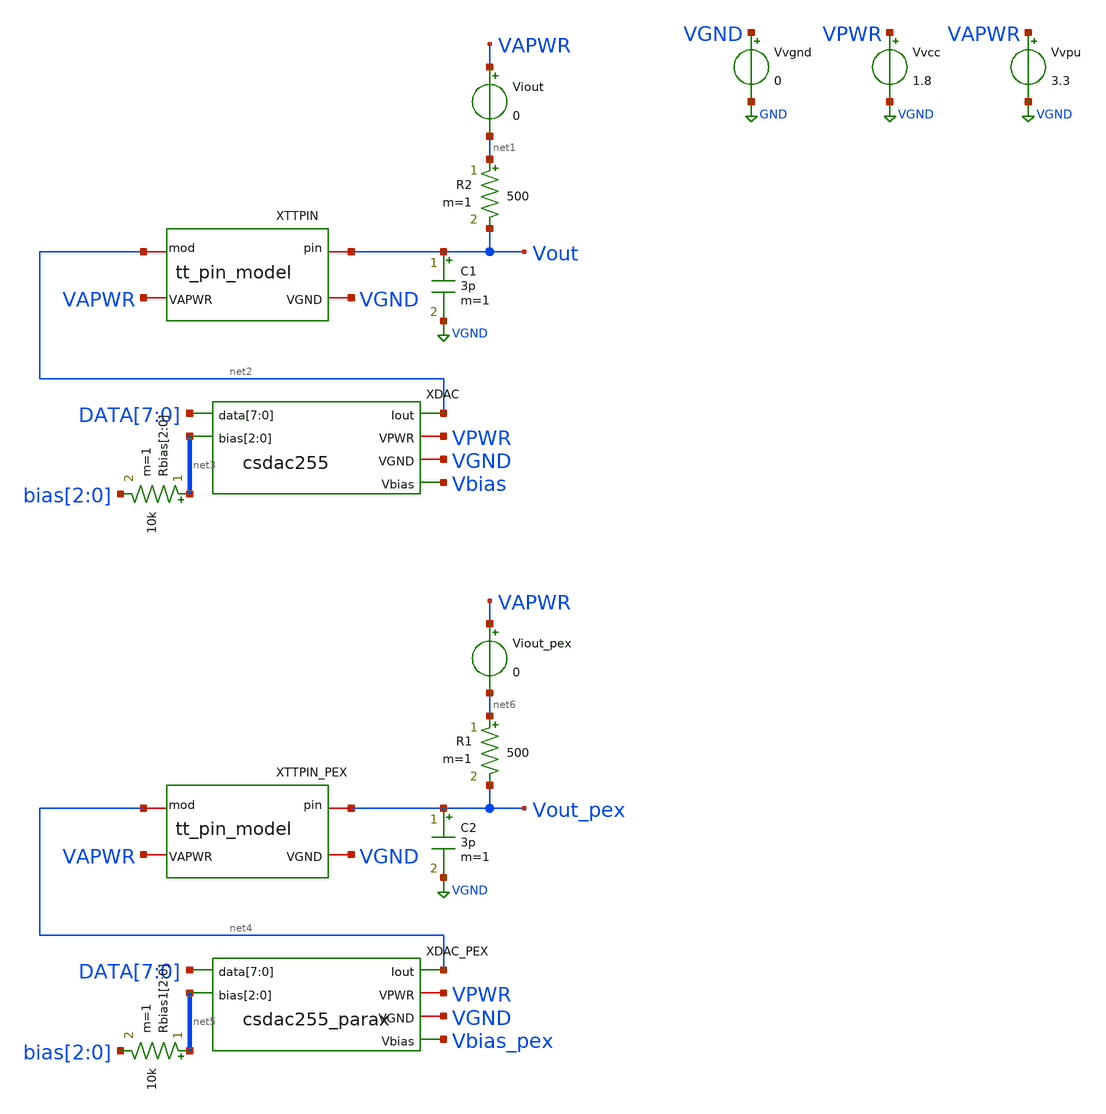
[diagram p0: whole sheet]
** sch_path: xschem/tb_csdac255.sch
**.subckt tb_csdac255
Vvcc VPWR VGND 1.8
Vvpu VAPWR VGND 3.3
Vvgnd VGND GND 0
XDAC DATA[7] DATA[6] DATA[5] DATA[4] DATA[3] DATA[2] DATA[1] DATA[0] net2 VPWR VGND Vbias net3[2]
+ net3[1] net3[0] csdac255
XTTPIN VGND VAPWR net2 Vout tt_pin_model
R2 net1 Vout 500 m=1
Viout VAPWR net1 0
C1 Vout VGND 3p m=1
Rbias[2] net3[2] bias[2] 10k m=1
Rbias[1] net3[1] bias[1] 10k m=1
Rbias[0] net3[0] bias[0] 10k m=1
XDAC_PEX DATA[7] DATA[6] DATA[5] DATA[4] DATA[3] DATA[2] DATA[1] DATA[0] net4 VPWR VGND Vbias_pex
+ net5[2] net5[1] net5[0] csdac255_parax
Rbias1[2] net5[2] bias[2] 10k m=1
Rbias1[1] net5[1] bias[1] 10k m=1
Rbias1[0] net5[0] bias[0] 10k m=1
XTTPIN_PEX VGND VAPWR net4 Vout_pex tt_pin_model
R1 net6 Vout_pex 500 m=1
Viout_pex VAPWR net6 0
C2 Vout_pex VGND 3p m=1
**** begin user architecture code



* Set Vbias level (negative logic, so 0=ON, 1.8=OFF):
.param bias2=1.8
.param bias1=1.8
.param bias0=1.8
Vvbias2 bias[2] GND {bias2}
Vvbias1 bias[1] GND {bias1}
Vvbias0 bias[0] GND {bias0}

*NOTE: Possible ngspice bug with .IF(), so it's commented out here:
*.param singlebits=0
*.IF (singlebits == 1)
* Mode to just test each binary-weighted level:
*Vxp0 DATA[0]  GND pulse 0v 1.8v 1u 1n 1n 1u 10u
*Vxp1 DATA[1]  GND pulse 0v 1.8v 2u 1n 1n 1u 10u
*Vxp2 DATA[2]  GND pulse 0v 1.8v 3u 1n 1n 1u 10u
*Vxp3 DATA[3]  GND pulse 0v 1.8v 4u 1n 1n 1u 10u
*Vxp4 DATA[4]  GND pulse 0v 1.8v 5u 1n 1n 1u 10u
*Vxp5 DATA[5]  GND pulse 0v 1.8v 6u 1n 1n 1u 10u
*Vxp6 DATA[6]  GND pulse 0v 1.8v 7u 1n 1n 1u 10u
*Vxp7 DATA[7]  GND pulse 0v 1.8v 8u 1n 1n 1u 10u
*.ELSEIF (singlebits == 0)
* Mode to test full 0..255 trange:
Vxp0 DATA[0]  GND pulse 1.8v 0v 0n 1n 1n 39n 80n
Vxp1 DATA[1]  GND pulse 1.8v 0v 0n 1n 1n 79n 160n
Vxp2 DATA[2]  GND pulse 1.8v 0v 0n 1n 1n 159n 320n
Vxp3 DATA[3]  GND pulse 1.8v 0v 0n 1n 1n 319n 640n
Vxp4 DATA[4]  GND pulse 1.8v 0v 0n 1n 1n 639n 1280n
Vxp5 DATA[5]  GND pulse 1.8v 0v 0n 1n 1n 1279n 2560n
Vxp6 DATA[6]  GND pulse 1.8v 0v 0n 1n 1n 2559n 5120n
Vxp7 DATA[7]  GND pulse 1.8v 0v 0n 1n 1n 5119n 10240n
*.endif

*.options savecurrents
.control
	* Start with all bias[*] switches at 0V (ENb), so highest Vbias (max current sink):
	let biaslevel=7
	foreach bv2 0 1.8
		foreach bv1 0 1.8
			foreach bv0 0 1.8
				alterparam bias2 = $bv2
				alterparam bias1 = $bv1
				alterparam bias0 = $bv0
				reset
				echo Bias level $&biaslevel = $bv2 $bv1 $bv0
				save
				+ data[0] data[1] data[2] data[3] data[4] data[5] data[6] data[7]
				+ bias[0] bias[1] bias[2]
				+ vbias          vbias_pex
				+ vout i(viout)  vout_pex i(viout_pex)
				+ i(vvcc)
				+ i(vvpu)
				+ i(vvgnd)
				+ XDAC.THERMO_ROWn[0] XDAC.THERMO_ROWn[1] XDAC.THERMO_ROWn[2] XDAC.THERMO_ROWn[3] XDAC.THERMO_ROWn[4] XDAC.THERMO_ROWn[5] XDAC.THERMO_ROWn[6] XDAC.THERMO_ROWn[7] XDAC.THERMO_ROWn[8] XDAC.THERMO_ROWn[9] XDAC.THERMO_ROWn[10] XDAC.THERMO_ROWn[11] XDAC.THERMO_ROWn[12] XDAC.THERMO_ROWn[13] XDAC.THERMO_ROWn[14]
				+ XDAC.THERMO_COLn[0] XDAC.THERMO_COLn[1] XDAC.THERMO_COLn[2] XDAC.THERMO_COLn[3] XDAC.THERMO_COLn[4] XDAC.THERMO_COLn[5] XDAC.THERMO_COLn[6] XDAC.THERMO_COLn[7] XDAC.THERMO_COLn[8] XDAC.THERMO_COLn[9] XDAC.THERMO_COLn[10] XDAC.THERMO_COLn[11] XDAC.THERMO_COLn[12] XDAC.THERMO_COLn[13] XDAC.THERMO_COLn[14]
				+ XDAC.XThR.TA1 XDAC.XThR.TA2 XDAC.XThR.TA3 XDAC.XThR.TAN XDAC.XThR.TAN2 XDAC.XThR.TB1 XDAC.XThR.TB2 XDAC.XThR.TB3 XDAC.XThR.TB4 XDAC.XThR.TB5 XDAC.XThR.TB6 XDAC.XThR.TB7 XDAC.XThR.TBN
				+ XDAC.XThC.TA1 XDAC.XThC.TA2 XDAC.XThC.TA3 XDAC.XThC.TAN XDAC.XThC.TAN2 XDAC.XThC.TB1 XDAC.XThC.TB2 XDAC.XThC.TB3 XDAC.XThC.TB4 XDAC.XThC.TB5 XDAC.XThC.TB6 XDAC.XThC.TB7 XDAC.XThC.TBN
				+ XDAC_PEX.XThR.Tn[0] XDAC_PEX.XThR.Tn[1] XDAC_PEX.XThR.Tn[2] XDAC_PEX.XThR.Tn[3] XDAC_PEX.XThR.Tn[4] XDAC_PEX.XThR.Tn[5] XDAC_PEX.XThR.Tn[6] XDAC_PEX.XThR.Tn[7] XDAC_PEX.XThR.Tn[8] XDAC_PEX.XThR.Tn[9] XDAC_PEX.XThR.Tn[10] XDAC_PEX.XThR.Tn[11] XDAC_PEX.XThR.Tn[12] XDAC_PEX.XThR.Tn[13] XDAC_PEX.XThR.Tn[14]
				+ XDAC_PEX.XThC.Tn[0] XDAC_PEX.XThC.Tn[1] XDAC_PEX.XThC.Tn[2] XDAC_PEX.XThC.Tn[3] XDAC_PEX.XThC.Tn[4] XDAC_PEX.XThC.Tn[5] XDAC_PEX.XThC.Tn[6] XDAC_PEX.XThC.Tn[7] XDAC_PEX.XThC.Tn[8] XDAC_PEX.XThC.Tn[9] XDAC_PEX.XThC.Tn[10] XDAC_PEX.XThC.Tn[11] XDAC_PEX.XThC.Tn[12] XDAC_PEX.XThC.Tn[13] XDAC_PEX.XThC.Tn[14]
				+ XDAC_PEX.XThR.TA1 XDAC_PEX.XThR.TA2 XDAC_PEX.XThR.TA3 XDAC_PEX.XThR.TAN XDAC_PEX.XThR.TAN2 XDAC_PEX.XThR.TB1 XDAC_PEX.XThR.TB2 XDAC_PEX.XThR.TB3 XDAC_PEX.XThR.TB4 XDAC_PEX.XThR.TB5 XDAC_PEX.XThR.TB6 XDAC_PEX.XThR.TB7 XDAC_PEX.XThR.TBN
				+ XDAC_PEX.XThC.TA1 XDAC_PEX.XThC.TA2 XDAC_PEX.XThC.TA3 XDAC_PEX.XThC.TAN XDAC_PEX.XThC.TAN2 XDAC_PEX.XThC.TB1 XDAC_PEX.XThC.TB2 XDAC_PEX.XThC.TB3 XDAC_PEX.XThC.TB4 XDAC_PEX.XThC.TB5 XDAC_PEX.XThC.TB6 XDAC_PEX.XThC.TB7 XDAC_PEX.XThC.TBN
				tran 1n 12.8u
				write tb_csdac255_all.raw
				write tb_csdac255.raw vbias vout i(viout) i(vvgnd) i(vvcc) i(vvpu) vbias_pex vout_pex i(viout_pex)
				+ XDAC.THERMO_ROWn[0] XDAC.THERMO_ROWn[1] XDAC.THERMO_ROWn[2] XDAC.THERMO_ROWn[3] XDAC.THERMO_ROWn[4] XDAC.THERMO_ROWn[5] XDAC.THERMO_ROWn[6] XDAC.THERMO_ROWn[7] XDAC.THERMO_ROWn[8] XDAC.THERMO_ROWn[9] XDAC.THERMO_ROWn[10] XDAC.THERMO_ROWn[11] XDAC.THERMO_ROWn[12] XDAC.THERMO_ROWn[13] XDAC.THERMO_ROWn[14] XDAC.THERMO_COLn[0] XDAC.THERMO_COLn[1] XDAC.THERMO_COLn[2] XDAC.THERMO_COLn[3] XDAC.THERMO_COLn[4] XDAC.THERMO_COLn[5] XDAC.THERMO_COLn[6] XDAC.THERMO_COLn[7] XDAC.THERMO_COLn[8] XDAC.THERMO_COLn[9] XDAC.THERMO_COLn[10] XDAC.THERMO_COLn[11] XDAC.THERMO_COLn[12] XDAC.THERMO_COLn[13] XDAC.THERMO_COLn[14] XDAC.XThR.TA1 XDAC.XThR.TA2 XDAC.XThR.TA3 XDAC.XThR.TAN XDAC.XThR.TAN2 XDAC.XThR.TB1 XDAC.XThR.TB2 XDAC.XThR.TB3 XDAC.XThR.TB4 XDAC.XThR.TB5 XDAC.XThR.TB6 XDAC.XThR.TB7 XDAC.XThR.TBN XDAC.XThC.TA1 XDAC.XThC.TA2 XDAC.XThC.TA3 XDAC.XThC.TAN XDAC.XThC.TAN2 XDAC.XThC.TB1 XDAC.XThC.TB2 XDAC.XThC.TB3 XDAC.XThC.TB4 XDAC.XThC.TB5 XDAC.XThC.TB6 XDAC.XThC.TB7 XDAC.XThC.TBN
				+ XDAC_PEX.XThR.Tn[0] XDAC_PEX.XThR.Tn[1] XDAC_PEX.XThR.Tn[2] XDAC_PEX.XThR.Tn[3] XDAC_PEX.XThR.Tn[4] XDAC_PEX.XThR.Tn[5] XDAC_PEX.XThR.Tn[6] XDAC_PEX.XThR.Tn[7] XDAC_PEX.XThR.Tn[8] XDAC_PEX.XThR.Tn[9] XDAC_PEX.XThR.Tn[10] XDAC_PEX.XThR.Tn[11] XDAC_PEX.XThR.Tn[12] XDAC_PEX.XThR.Tn[13] XDAC_PEX.XThR.Tn[14] XDAC_PEX.XThC.Tn[0] XDAC_PEX.XThC.Tn[1] XDAC_PEX.XThC.Tn[2] XDAC_PEX.XThC.Tn[3] XDAC_PEX.XThC.Tn[4] XDAC_PEX.XThC.Tn[5] XDAC_PEX.XThC.Tn[6] XDAC_PEX.XThC.Tn[7] XDAC_PEX.XThC.Tn[8] XDAC_PEX.XThC.Tn[9] XDAC_PEX.XThC.Tn[10] XDAC_PEX.XThC.Tn[11] XDAC_PEX.XThC.Tn[12] XDAC_PEX.XThC.Tn[13] XDAC_PEX.XThC.Tn[14] XDAC_PEX.XThR.TA1 XDAC_PEX.XThR.TA2 XDAC_PEX.XThR.TA3 XDAC_PEX.XThR.TAN XDAC_PEX.XThR.TAN2 XDAC_PEX.XThR.TB1 XDAC_PEX.XThR.TB2 XDAC_PEX.XThR.TB3 XDAC_PEX.XThR.TB4 XDAC_PEX.XThR.TB5 XDAC_PEX.XThR.TB6 XDAC_PEX.XThR.TB7 XDAC_PEX.XThR.TBN XDAC_PEX.XThC.TA1 XDAC_PEX.XThC.TA2 XDAC_PEX.XThC.TA3 XDAC_PEX.XThC.TAN XDAC_PEX.XThC.TAN2 XDAC_PEX.XThC.TB1 XDAC_PEX.XThC.TB2 XDAC_PEX.XThC.TB3 XDAC_PEX.XThC.TB4 XDAC_PEX.XThC.TB5 XDAC_PEX.XThC.TB6 XDAC_PEX.XThC.TB7 XDAC_PEX.XThC.TBN
				*plot vout vbias i(viout)*1000
				set appendwrite
				reset
				let biaslevel = biaslevel - 1
			end
		end
	end
.endc




.lib /home/anton/asic/ciel/sky130A/libs.tech/combined/sky130.lib.spice tt
.include $::SKYWATER_STDCELLS/sky130_fd_sc_hd.spice

**** end user architecture code
**.ends

* expanding   symbol:  csdac255.sym # of pins=6
** sym_path: xschem/csdac255.sym
** sch_path: xschem/csdac255.sch
.subckt csdac255 data[7] data[6] data[5] data[4] data[3] data[2] data[1] data[0] Iout VPWR VGND Vbias bias[2] bias[1] bias[0]
*.iopin VPWR
*.opin Iout
*.iopin VGND
*.ipin bias[2],bias[1],bias[0]
*.ipin data[7],data[6],data[5],data[4],data[3],data[2],data[1],data[0]
*.opin Vbias
XThR VPWR VGND THERMO_ROWn[14] THERMO_ROWn[13] THERMO_ROWn[12] THERMO_ROWn[11] THERMO_ROWn[10] THERMO_ROWn[9] THERMO_ROWn[8] THERMO_ROWn[7] THERMO_ROWn[6] THERMO_ROWn[5] THERMO_ROWn[4] THERMO_ROWn[3] THERMO_ROWn[2] THERMO_ROWn[1] THERMO_ROWn[0] data[7] data[6] data[5] data[4] thermo15
XA VPWR VGND THERMO_ROWn[14] THERMO_ROWn[13] THERMO_ROWn[12] THERMO_ROWn[11] THERMO_ROWn[10] THERMO_ROWn[9] THERMO_ROWn[8] THERMO_ROWn[7] THERMO_ROWn[6] THERMO_ROWn[5] THERMO_ROWn[4] THERMO_ROWn[3] THERMO_ROWn[2] THERMO_ROWn[1] THERMO_ROWn[0] THERMO_COLn[14] THERMO_COLn[13] THERMO_COLn[12] THERMO_COLn[11] THERMO_COLn[10] THERMO_COLn[9] THERMO_COLn[8] THERMO_COLn[7] THERMO_COLn[6] THERMO_COLn[5] THERMO_COLn[4] THERMO_COLn[3] THERMO_COLn[2] THERMO_COLn[1] THERMO_COLn[0] Vbias Iout array255x
XThC VPWR VGND THERMO_COLn[14] THERMO_COLn[13] THERMO_COLn[12] THERMO_COLn[11] THERMO_COLn[10] THERMO_COLn[9] THERMO_COLn[8] THERMO_COLn[7] THERMO_COLn[6] THERMO_COLn[5] THERMO_COLn[4] THERMO_COLn[3] THERMO_COLn[2] THERMO_COLn[1] THERMO_COLn[0] data[3] data[2] data[1] data[0] thermo15
XVB VPWR VGND bias[2] bias[1] bias[0] Vbias vbias
XCVb Vbias VGND sky130_fd_pr__cap_mim_m3_1 W=11.82 L=4.81 MF=1 m=1
.ends


* expanding   symbol:  tt_pin_model.sym # of pins=4
** sym_path: xschem/tt_pin_model.sym
** sch_path: xschem/tt_pin_model.sch
.subckt tt_pin_model VGND VAPWR mod pin
*.iopin VGND
*.iopin VAPWR
*.iopin mod
*.iopin pin
R2 net1 pin 1 m=1
C2 pin VGND 1p m=1
L7 net2 net1 1n m=1
C3 net2 VGND 2p m=1
R3 net3 net2 50 m=1
C4 net3 VGND 250f m=1
XM2 net3 VGND mod VAPWR sky130_fd_pr__pfet_g5v0d10v5 L=0.5 W=100 nf=20 ad='int((nf+1)/2) * W/nf * 0.29' as='int((nf+2)/2)
+ * W/nf * 0.29' pd='2*int((nf+1)/2) * (W/nf + 0.29)' ps='2*int((nf+2)/2) * (W/nf + 0.29)' nrd='0.29 /
+ W' nrs='0.29 / W' sa=0 sb=0 sd=0 mult=1 m=1
XM1 net3 VAPWR mod VGND sky130_fd_pr__nfet_g5v0d10v5 L=0.5 W=60 nf=12 ad='int((nf+1)/2) * W/nf * 0.29' as='int((nf+2)/2)
+ * W/nf * 0.29' pd='2*int((nf+1)/2) * (W/nf + 0.29)' ps='2*int((nf+2)/2) * (W/nf + 0.29)' nrd='0.29 /
+ W' nrs='0.29 / W' sa=0 sb=0 sd=0 mult=1 m=1
XM4 net3 VAPWR VGND VAPWR sky130_fd_pr__pfet_g5v0d10v5 L=0.5 W=100 nf=20 ad='int((nf+1)/2) * W/nf * 0.29' as='int((nf+2)/2)
+ * W/nf * 0.29' pd='2*int((nf+1)/2) * (W/nf + 0.29)' ps='2*int((nf+2)/2) * (W/nf + 0.29)' nrd='0.29 /
+ W' nrs='0.29 / W' sa=0 sb=0 sd=0 mult=15 m=15
XM3 net3 VGND VGND VGND sky130_fd_pr__nfet_g5v0d10v5 L=0.5 W=60 nf=12 ad='int((nf+1)/2) * W/nf * 0.29' as='int((nf+2)/2)
+ * W/nf * 0.29' pd='2*int((nf+1)/2) * (W/nf + 0.29)' ps='2*int((nf+2)/2) * (W/nf + 0.29)' nrd='0.29 /
+ W' nrs='0.29 / W' sa=0 sb=0 sd=0 mult=15 m=15
C5 mod VGND 250f m=1
.ends


* expanding   symbol:  csdac255_parax.sym # of pins=6
** sym_path: xschem/csdac255.sym
.include [file normalize ../mag/csdac255.sim.spice]

* expanding   symbol:  thermo15.sym # of pins=4
** sym_path: xschem/thermo15.sym
** sch_path: xschem/thermo15.sch
.subckt thermo15 VPWR VGND Tn[14] Tn[13] Tn[12] Tn[11] Tn[10] Tn[9] Tn[8] Tn[7] Tn[6] Tn[5] Tn[4] Tn[3] Tn[2] Tn[1] Tn[0] d[3] d[2] d[1] d[0]
*.iopin VPWR
*.ipin d[3],d[2],d[1],d[0]
*.iopin VGND
*.opin Tn[14],Tn[13],Tn[12],Tn[11],Tn[10],Tn[9],Tn[8],Tn[7],Tn[6],Tn[5],Tn[4],Tn[3],Tn[2],Tn[1],Tn[0]
XTA2 d[1] VGND VGND VPWR VPWR TA2 sky130_fd_sc_hd__inv_1
XTBN TAN2 VGND VGND VPWR VPWR TBN sky130_fd_sc_hd__inv_2
XTA3 d[0] d[1] VGND VGND VPWR VPWR TA3 sky130_fd_sc_hd__nand2_1
XTA1 d[0] d[1] VGND VGND VPWR VPWR TA1 sky130_fd_sc_hd__nor2_1
XTAN d[2] VGND VGND VPWR VPWR TAN sky130_fd_sc_hd__inv_1
XTB1 TA1 TAN VGND VGND VPWR VPWR TB1 sky130_fd_sc_hd__nand2_1
XTB2 TA2 TAN VGND VGND VPWR VPWR TB2 sky130_fd_sc_hd__nand2_1
XTB3 TA3 TAN VGND VGND VPWR VPWR TB3 sky130_fd_sc_hd__nand2_1
XTB4 TAN VGND VGND VPWR VPWR TB4 sky130_fd_sc_hd__inv_1
XTB5 TA1 TAN VGND VGND VPWR VPWR TB5 sky130_fd_sc_hd__nor2_1
XTB6 TA2 TAN VGND VGND VPWR VPWR TB6 sky130_fd_sc_hd__nor2_1
XTB7 TA3 TAN VGND VGND VPWR VPWR TB7 sky130_fd_sc_hd__nor2_1
XOTn0 TB1 TBN VGND VGND VPWR VPWR Tn[0] sky130_fd_sc_hd__nor2_4
XOTn1 TB2 TBN VGND VGND VPWR VPWR Tn[1] sky130_fd_sc_hd__nor2_4
XOTn2 TB3 TBN VGND VGND VPWR VPWR Tn[2] sky130_fd_sc_hd__nor2_4
XOTn3 TB4 TBN VGND VGND VPWR VPWR Tn[3] sky130_fd_sc_hd__nor2_4
XOTn4 TB5 TBN VGND VGND VPWR VPWR Tn[4] sky130_fd_sc_hd__nor2_4
XOTn5 TB6 TBN VGND VGND VPWR VPWR Tn[5] sky130_fd_sc_hd__nor2_4
XOTn6 TB7 TBN VGND VGND VPWR VPWR Tn[6] sky130_fd_sc_hd__nor2_4
XOTn7 TBN VGND VGND VPWR VPWR Tn[7] sky130_fd_sc_hd__inv_4
XOTn8 TB1 TBN VGND VGND VPWR VPWR Tn[8] sky130_fd_sc_hd__nand2_4
XOTn9 TB2 TBN VGND VGND VPWR VPWR Tn[9] sky130_fd_sc_hd__nand2_4
XOTn10 TB3 TBN VGND VGND VPWR VPWR Tn[10] sky130_fd_sc_hd__nand2_4
XOTn11 TB4 TBN VGND VGND VPWR VPWR Tn[11] sky130_fd_sc_hd__nand2_4
XOTn12 TB5 TBN VGND VGND VPWR VPWR Tn[12] sky130_fd_sc_hd__nand2_4
XOTn13 TB6 TBN VGND VGND VPWR VPWR Tn[13] sky130_fd_sc_hd__nand2_4
XOTn14 TB7 TBN VGND VGND VPWR VPWR Tn[14] sky130_fd_sc_hd__nand2_4
XTAN2 d[3] VGND VGND VPWR VPWR TAN2 sky130_fd_sc_hd__inv_1
.ends


* expanding   symbol:  array255x.sym # of pins=6
** sym_path: xschem/array255x.sym
** sch_path: xschem/array255x.sch
.subckt array255x VPWR VGND Rn[14] Rn[13] Rn[12] Rn[11] Rn[10] Rn[9] Rn[8] Rn[7] Rn[6] Rn[5] Rn[4] Rn[3] Rn[2] Rn[1] Rn[0] Cn[14] Cn[13] Cn[12] Cn[11] Cn[10] Cn[9] Cn[8] Cn[7] Cn[6] Cn[5] Cn[4] Cn[3] Cn[2] Cn[1] Cn[0] Vbias Iout
*.iopin VPWR
*.opin Iout
*.iopin VGND
*.ipin Vbias
*.ipin Cn[14],Cn[13],Cn[12],Cn[11],Cn[10],Cn[9],Cn[8],Cn[7],Cn[6],Cn[5],Cn[4],Cn[3],Cn[2],Cn[1],Cn[0]
*.ipin Rn[14],Rn[13],Rn[12],Rn[11],Rn[10],Rn[9],Rn[8],Rn[7],Rn[6],Rn[5],Rn[4],Rn[3],Rn[2],Rn[1],Rn[0]
XIR[14] Vbias VPWR Rn[14] Rn[13] Cn[14] Cn[13] Cn[12] Cn[11] Cn[10] Cn[9] Cn[8] Cn[7] Cn[6] Cn[5] Cn[4] Cn[3] Cn[2] Cn[1] Cn[0] VGND Iout row15x
XIR[13] Vbias VPWR Rn[13] Rn[12] Cn[14] Cn[13] Cn[12] Cn[11] Cn[10] Cn[9] Cn[8] Cn[7] Cn[6] Cn[5] Cn[4] Cn[3] Cn[2] Cn[1] Cn[0] VGND Iout row15x
XIR[12] Vbias VPWR Rn[12] Rn[11] Cn[14] Cn[13] Cn[12] Cn[11] Cn[10] Cn[9] Cn[8] Cn[7] Cn[6] Cn[5] Cn[4] Cn[3] Cn[2] Cn[1] Cn[0] VGND Iout row15x
XIR[11] Vbias VPWR Rn[11] Rn[10] Cn[14] Cn[13] Cn[12] Cn[11] Cn[10] Cn[9] Cn[8] Cn[7] Cn[6] Cn[5] Cn[4] Cn[3] Cn[2] Cn[1] Cn[0] VGND Iout row15x
XIR[10] Vbias VPWR Rn[10] Rn[9] Cn[14] Cn[13] Cn[12] Cn[11] Cn[10] Cn[9] Cn[8] Cn[7] Cn[6] Cn[5] Cn[4] Cn[3] Cn[2] Cn[1] Cn[0] VGND Iout row15x
XIR[9] Vbias VPWR Rn[9] Rn[8] Cn[14] Cn[13] Cn[12] Cn[11] Cn[10] Cn[9] Cn[8] Cn[7] Cn[6] Cn[5] Cn[4] Cn[3] Cn[2] Cn[1] Cn[0] VGND Iout row15x
XIR[8] Vbias VPWR Rn[8] Rn[7] Cn[14] Cn[13] Cn[12] Cn[11] Cn[10] Cn[9] Cn[8] Cn[7] Cn[6] Cn[5] Cn[4] Cn[3] Cn[2] Cn[1] Cn[0] VGND Iout row15x
XIR[7] Vbias VPWR Rn[7] Rn[6] Cn[14] Cn[13] Cn[12] Cn[11] Cn[10] Cn[9] Cn[8] Cn[7] Cn[6] Cn[5] Cn[4] Cn[3] Cn[2] Cn[1] Cn[0] VGND Iout row15x
XIR[6] Vbias VPWR Rn[6] Rn[5] Cn[14] Cn[13] Cn[12] Cn[11] Cn[10] Cn[9] Cn[8] Cn[7] Cn[6] Cn[5] Cn[4] Cn[3] Cn[2] Cn[1] Cn[0] VGND Iout row15x
XIR[5] Vbias VPWR Rn[5] Rn[4] Cn[14] Cn[13] Cn[12] Cn[11] Cn[10] Cn[9] Cn[8] Cn[7] Cn[6] Cn[5] Cn[4] Cn[3] Cn[2] Cn[1] Cn[0] VGND Iout row15x
XIR[4] Vbias VPWR Rn[4] Rn[3] Cn[14] Cn[13] Cn[12] Cn[11] Cn[10] Cn[9] Cn[8] Cn[7] Cn[6] Cn[5] Cn[4] Cn[3] Cn[2] Cn[1] Cn[0] VGND Iout row15x
XIR[3] Vbias VPWR Rn[3] Rn[2] Cn[14] Cn[13] Cn[12] Cn[11] Cn[10] Cn[9] Cn[8] Cn[7] Cn[6] Cn[5] Cn[4] Cn[3] Cn[2] Cn[1] Cn[0] VGND Iout row15x
XIR[2] Vbias VPWR Rn[2] Rn[1] Cn[14] Cn[13] Cn[12] Cn[11] Cn[10] Cn[9] Cn[8] Cn[7] Cn[6] Cn[5] Cn[4] Cn[3] Cn[2] Cn[1] Cn[0] VGND Iout row15x
XIR[1] Vbias VPWR Rn[1] Rn[0] Cn[14] Cn[13] Cn[12] Cn[11] Cn[10] Cn[9] Cn[8] Cn[7] Cn[6] Cn[5] Cn[4] Cn[3] Cn[2] Cn[1] Cn[0] VGND Iout row15x
XIR[0] Vbias VPWR Rn[0] VGND Cn[14] Cn[13] Cn[12] Cn[11] Cn[10] Cn[9] Cn[8] Cn[7] Cn[6] Cn[5] Cn[4] Cn[3] Cn[2] Cn[1] Cn[0] VGND Iout row15x
XIR[15] Vbias VPWR VPWR Rn[14] Cn[14] Cn[13] Cn[12] Cn[11] Cn[10] Cn[9] Cn[8] Cn[7] Cn[6] Cn[5] Cn[4] Cn[3] Cn[2] Cn[1] Cn[0] VGND Iout row15x
.ends


* expanding   symbol:  vbias.sym # of pins=4
** sym_path: xschem/vbias.sym
** sch_path: xschem/vbias.sch
.subckt vbias VPWR VGND bias[2] bias[1] bias[0] Vbias
*.iopin VPWR
*.iopin VGND
*.ipin bias[2],bias[1],bias[0]
*.opin Vbias
XM1 Vbias bias[2] VPWR VPWR sky130_fd_pr__pfet_01v8 L=0.35 W=2 nf=1 ad='int((nf+1)/2) * W/nf * 0.29' as='int((nf+2)/2)
+ * W/nf * 0.29' pd='2*int((nf+1)/2) * (W/nf + 0.29)' ps='2*int((nf+2)/2) * (W/nf + 0.29)' nrd='0.29 /
+ W' nrs='0.29 / W' sa=0 sb=0 sd=0 mult=1 m=1
XM2 Vbias bias[1] VPWR VPWR sky130_fd_pr__pfet_01v8 L=0.7 W=2 nf=1 ad='int((nf+1)/2) * W/nf * 0.29' as='int((nf+2)/2)
+ * W/nf * 0.29' pd='2*int((nf+1)/2) * (W/nf + 0.29)' ps='2*int((nf+2)/2) * (W/nf + 0.29)' nrd='0.29 /
+ W' nrs='0.29 / W' sa=0 sb=0 sd=0 mult=1 m=1
XM3 Vbias bias[0] VPWR VPWR sky130_fd_pr__pfet_01v8 L=1.4 W=2 nf=1 ad='int((nf+1)/2) * W/nf * 0.29' as='int((nf+2)/2)
+ * W/nf * 0.29' pd='2*int((nf+1)/2) * (W/nf + 0.29)' ps='2*int((nf+2)/2) * (W/nf + 0.29)' nrd='0.29 /
+ W' nrs='0.29 / W' sa=0 sb=0 sd=0 mult=1 m=1
XMmirror Vbias Vbias VGND VGND sky130_fd_pr__nfet_g5v0d10v5 L=0.5 W=7.5 nf=1 ad='int((nf+1)/2) * W/nf
+ * 0.29' as='int((nf+2)/2) * W/nf * 0.29' pd='2*int((nf+1)/2) * (W/nf + 0.29)' ps='2*int((nf+2)/2) * (W/nf
+ + 0.29)' nrd='0.29 / W' nrs='0.29 / W' sa=0 sb=0 sd=0 mult=1 m=1
XM4 Vbias VGND VPWR VPWR sky130_fd_pr__pfet_01v8 L=1.4 W=2 nf=1 ad='int((nf+1)/2) * W/nf * 0.29' as='int((nf+2)/2)
+ * W/nf * 0.29' pd='2*int((nf+1)/2) * (W/nf + 0.29)' ps='2*int((nf+2)/2) * (W/nf + 0.29)' nrd='0.29 /
+ W' nrs='0.29 / W' sa=0 sb=0 sd=0 mult=1 m=1
.ends


* expanding   symbol:  row15x.sym # of pins=7
** sym_path: xschem/row15x.sym
** sch_path: xschem/row15x.sch
.subckt row15x Vbias VPWR Sn Rn Cn[14] Cn[13] Cn[12] Cn[11] Cn[10] Cn[9] Cn[8] Cn[7] Cn[6] Cn[5] Cn[4] Cn[3] Cn[2] Cn[1] Cn[0] VGND Iout
*.ipin Sn
*.ipin Rn
*.ipin Cn[14],Cn[13],Cn[12],Cn[11],Cn[10],Cn[9],Cn[8],Cn[7],Cn[6],Cn[5],Cn[4],Cn[3],Cn[2],Cn[1],Cn[0]
*.iopin VPWR
*.iopin VGND
*.opin Iout
*.ipin Vbias
XIC[14] VPWR VGND Rn Cn[14] Sn Vbias Iout icell
XIC[13] VPWR VGND Rn Cn[13] Sn Vbias Iout icell
XIC[12] VPWR VGND Rn Cn[12] Sn Vbias Iout icell
XIC[11] VPWR VGND Rn Cn[11] Sn Vbias Iout icell
XIC[10] VPWR VGND Rn Cn[10] Sn Vbias Iout icell
XIC[9] VPWR VGND Rn Cn[9] Sn Vbias Iout icell
XIC[8] VPWR VGND Rn Cn[8] Sn Vbias Iout icell
XIC[7] VPWR VGND Rn Cn[7] Sn Vbias Iout icell
XIC[6] VPWR VGND Rn Cn[6] Sn Vbias Iout icell
XIC[5] VPWR VGND Rn Cn[5] Sn Vbias Iout icell
XIC[4] VPWR VGND Rn Cn[4] Sn Vbias Iout icell
XIC[3] VPWR VGND Rn Cn[3] Sn Vbias Iout icell
XIC[2] VPWR VGND Rn Cn[2] Sn Vbias Iout icell
XIC[1] VPWR VGND Rn Cn[1] Sn Vbias Iout icell
XIC[0] VPWR VGND Rn Cn[0] Sn Vbias Iout icell
XIC[15] VPWR VGND VPWR VPWR Sn Vbias Iout icell
XIC_dummy_left VPWR VGND VPWR VPWR VPWR VGND net1 icell
XIC_dummy_right VPWR VGND VPWR VPWR VPWR VGND net2 icell
.ends


* expanding   symbol:  icell.sym # of pins=7
** sym_path: xschem/icell.sym
** sch_path: xschem/icell.sch
.subckt icell VPWR VGND Rn Cn Sn Vbias Iout
*.ipin Rn
*.iopin VPWR
*.opin Iout
*.iopin VGND
*.ipin Cn
*.ipin Sn
*.ipin Vbias
XM2 Ien Sn VPWR VPWR sky130_fd_pr__pfet_01v8 L=0.15 W=0.5 nf=1 ad='int((nf+1)/2) * W/nf * 0.29' as='int((nf+2)/2)
+ * W/nf * 0.29' pd='2*int((nf+1)/2) * (W/nf + 0.29)' ps='2*int((nf+2)/2) * (W/nf + 0.29)' nrd='0.29 /
+ W' nrs='0.29 / W' sa=0 sb=0 sd=0 mult=1 m=1
XM3 Ien Sn PDM VGND sky130_fd_pr__nfet_01v8 L=0.15 W=0.5 nf=1 ad='int((nf+1)/2) * W/nf * 0.29' as='int((nf+2)/2)
+ * W/nf * 0.29' pd='2*int((nf+1)/2) * (W/nf + 0.29)' ps='2*int((nf+2)/2) * (W/nf + 0.29)' nrd='0.29 /
+ W' nrs='0.29 / W' sa=0 sb=0 sd=0 mult=1 m=1
XM4 Ien Cn PUM VPWR sky130_fd_pr__pfet_01v8 L=0.15 W=0.5 nf=1 ad='int((nf+1)/2) * W/nf * 0.29' as='int((nf+2)/2)
+ * W/nf * 0.29' pd='2*int((nf+1)/2) * (W/nf + 0.29)' ps='2*int((nf+2)/2) * (W/nf + 0.29)' nrd='0.29 /
+ W' nrs='0.29 / W' sa=0 sb=0 sd=0 mult=1 m=1
XM5 PUM Rn VPWR VPWR sky130_fd_pr__pfet_01v8 L=0.15 W=0.5 nf=1 ad='int((nf+1)/2) * W/nf * 0.29' as='int((nf+2)/2)
+ * W/nf * 0.29' pd='2*int((nf+1)/2) * (W/nf + 0.29)' ps='2*int((nf+2)/2) * (W/nf + 0.29)' nrd='0.29 /
+ W' nrs='0.29 / W' sa=0 sb=0 sd=0 mult=1 m=1
XM6 PDM Rn VGND VGND sky130_fd_pr__nfet_01v8 L=0.15 W=0.5 nf=1 ad='int((nf+1)/2) * W/nf * 0.29' as='int((nf+2)/2)
+ * W/nf * 0.29' pd='2*int((nf+1)/2) * (W/nf + 0.29)' ps='2*int((nf+2)/2) * (W/nf + 0.29)' nrd='0.29 /
+ W' nrs='0.29 / W' sa=0 sb=0 sd=0 mult=1 m=1
XM7 PDM Cn VGND VGND sky130_fd_pr__nfet_01v8 L=0.15 W=0.5 nf=1 ad='int((nf+1)/2) * W/nf * 0.29' as='int((nf+2)/2)
+ * W/nf * 0.29' pd='2*int((nf+1)/2) * (W/nf + 0.29)' ps='2*int((nf+2)/2) * (W/nf + 0.29)' nrd='0.29 /
+ W' nrs='0.29 / W' sa=0 sb=0 sd=0 mult=1 m=1
XM1 SM Vbias VGND VGND sky130_fd_pr__nfet_g5v0d10v5 L=0.5 W=0.5 nf=1 ad='int((nf+1)/2) * W/nf * 0.29' as='int((nf+2)/2)
+ * W/nf * 0.29' pd='2*int((nf+1)/2) * (W/nf + 0.29)' ps='2*int((nf+2)/2) * (W/nf + 0.29)' nrd='0.29 /
+ W' nrs='0.29 / W' sa=0 sb=0 sd=0 mult=1 m=1
XM8 Iout Ien SM VGND sky130_fd_pr__nfet_g5v0d10v5 L=0.5 W=1.0 nf=1 ad='int((nf+1)/2) * W/nf * 0.29' as='int((nf+2)/2)
+ * W/nf * 0.29' pd='2*int((nf+1)/2) * (W/nf + 0.29)' ps='2*int((nf+2)/2) * (W/nf + 0.29)' nrd='0.29 /
+ W' nrs='0.29 / W' sa=0 sb=0 sd=0 mult=1 m=1
.ends

.GLOBAL GND
.GLOBAL VGND
.end
